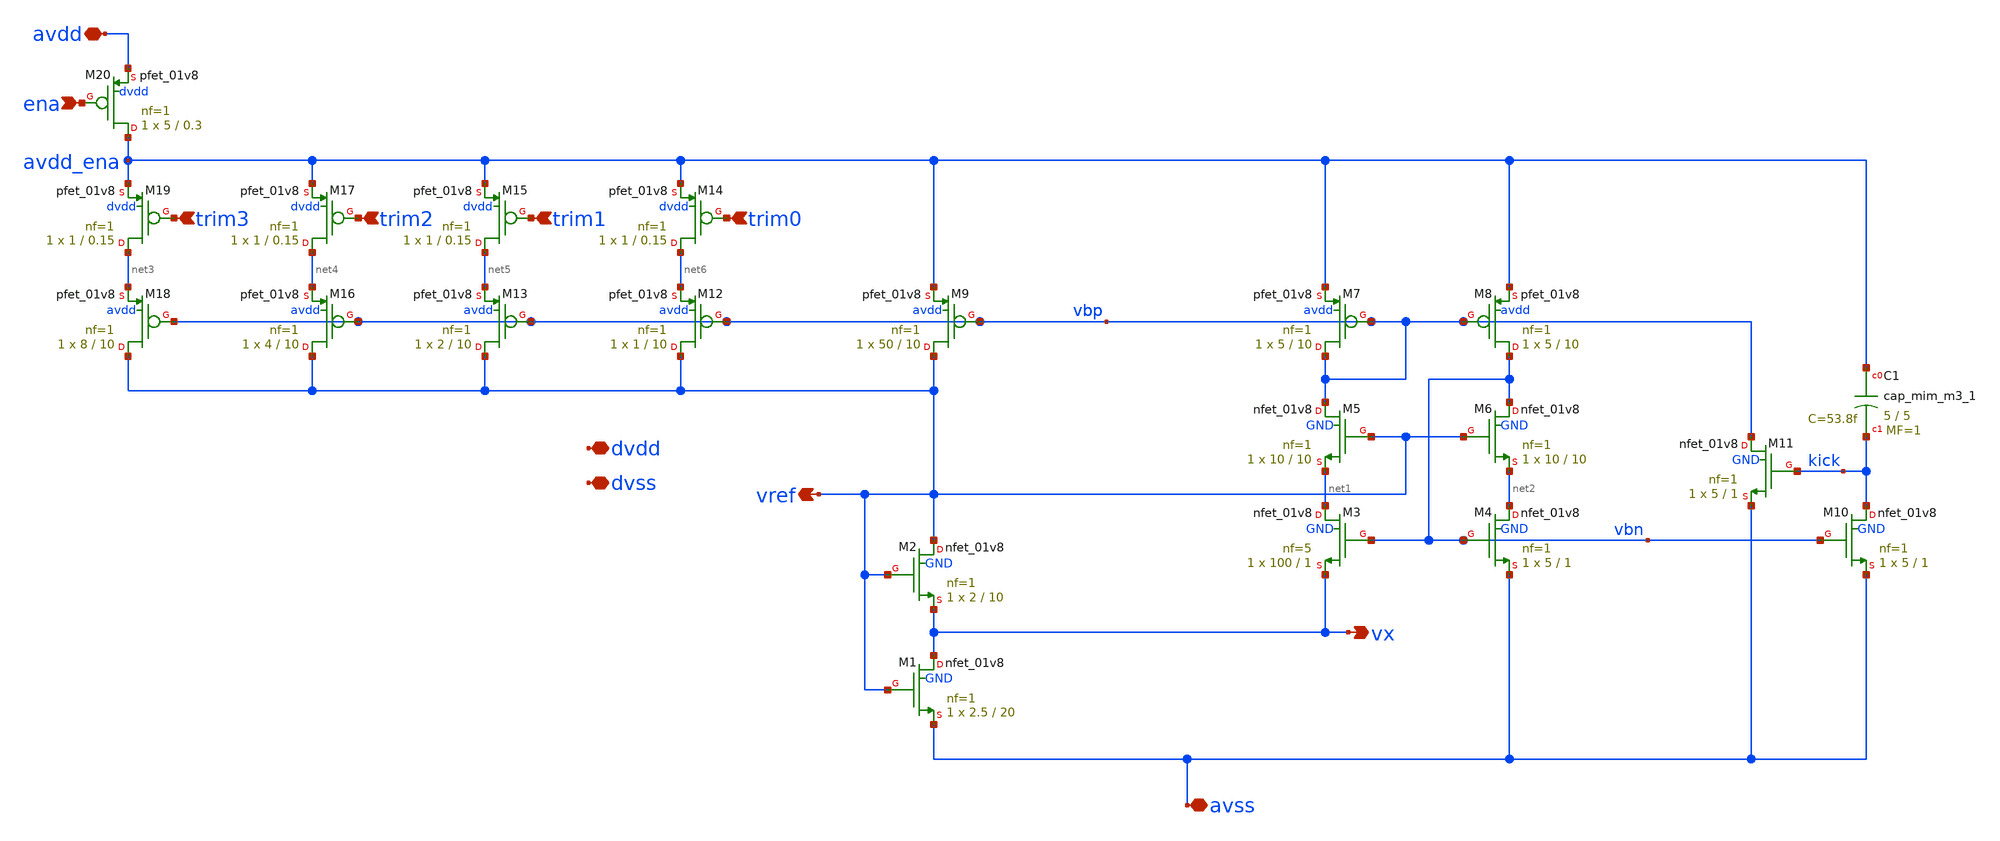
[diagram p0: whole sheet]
** sch_path: xschem/sky130_ak_ip__cmos_vref.sch
**.subckt sky130_ak_ip__cmos_vref vref avss avdd vx trim0 trim1 trim2 trim3 dvdd dvss ena
*.opin vref
*.iopin avss
*.iopin avdd
*.opin vx
*.ipin trim0
*.ipin trim1
*.ipin trim2
*.ipin trim3
*.iopin dvdd
*.iopin dvss
*.ipin ena
XM2 vref vref vx GND sky130_fd_pr__nfet_01v8 L=10 W=2 nf=1 ad='int((nf+1)/2) * W/nf * 0.29' as='int((nf+2)/2) * W/nf * 0.29'
+ pd='2*int((nf+1)/2) * (W/nf + 0.29)' ps='2*int((nf+2)/2) * (W/nf + 0.29)' nrd='0.29 / W' nrs='0.29 / W'
+ sa=0 sb=0 sd=0 mult=1 m=1
XM1 vx vref avss GND sky130_fd_pr__nfet_01v8 L=20 W=2.5 nf=1 ad='int((nf+1)/2) * W/nf * 0.29' as='int((nf+2)/2) * W/nf * 0.29'
+ pd='2*int((nf+1)/2) * (W/nf + 0.29)' ps='2*int((nf+2)/2) * (W/nf + 0.29)' nrd='0.29 / W' nrs='0.29 / W'
+ sa=0 sb=0 sd=0 mult=1 m=1
XM3 net1 vbn vx GND sky130_fd_pr__nfet_01v8 L=1 W=100 nf=5 ad='int((nf+1)/2) * W/nf * 0.29' as='int((nf+2)/2) * W/nf * 0.29'
+ pd='2*int((nf+1)/2) * (W/nf + 0.29)' ps='2*int((nf+2)/2) * (W/nf + 0.29)' nrd='0.29 / W' nrs='0.29 / W'
+ sa=0 sb=0 sd=0 mult=1 m=1
XM4 net2 vbn avss GND sky130_fd_pr__nfet_01v8 L=1 W=5 nf=1 ad='int((nf+1)/2) * W/nf * 0.29' as='int((nf+2)/2) * W/nf * 0.29'
+ pd='2*int((nf+1)/2) * (W/nf + 0.29)' ps='2*int((nf+2)/2) * (W/nf + 0.29)' nrd='0.29 / W' nrs='0.29 / W'
+ sa=0 sb=0 sd=0 mult=1 m=1
XM5 vbp vref net1 GND sky130_fd_pr__nfet_01v8 L=10 W=10 nf=1 ad='int((nf+1)/2) * W/nf * 0.29' as='int((nf+2)/2) * W/nf * 0.29'
+ pd='2*int((nf+1)/2) * (W/nf + 0.29)' ps='2*int((nf+2)/2) * (W/nf + 0.29)' nrd='0.29 / W' nrs='0.29 / W'
+ sa=0 sb=0 sd=0 mult=1 m=1
XM6 vbn vref net2 GND sky130_fd_pr__nfet_01v8 L=10 W=10 nf=1 ad='int((nf+1)/2) * W/nf * 0.29' as='int((nf+2)/2) * W/nf * 0.29'
+ pd='2*int((nf+1)/2) * (W/nf + 0.29)' ps='2*int((nf+2)/2) * (W/nf + 0.29)' nrd='0.29 / W' nrs='0.29 / W'
+ sa=0 sb=0 sd=0 mult=1 m=1
XM7 vbp vbp avdd_ena avdd sky130_fd_pr__pfet_01v8 L=10 W=5 nf=1 ad='int((nf+1)/2) * W/nf * 0.29' as='int((nf+2)/2) * W/nf * 0.29'
+ pd='2*int((nf+1)/2) * (W/nf + 0.29)' ps='2*int((nf+2)/2) * (W/nf + 0.29)' nrd='0.29 / W' nrs='0.29 / W'
+ sa=0 sb=0 sd=0 mult=1 m=1
XM8 vbn vbp avdd_ena avdd sky130_fd_pr__pfet_01v8 L=10 W=5 nf=1 ad='int((nf+1)/2) * W/nf * 0.29' as='int((nf+2)/2) * W/nf * 0.29'
+ pd='2*int((nf+1)/2) * (W/nf + 0.29)' ps='2*int((nf+2)/2) * (W/nf + 0.29)' nrd='0.29 / W' nrs='0.29 / W'
+ sa=0 sb=0 sd=0 mult=1 m=1
XM9 vref vbp avdd_ena avdd sky130_fd_pr__pfet_01v8 L=10 W=50 nf=1 ad='int((nf+1)/2) * W/nf * 0.29' as='int((nf+2)/2) * W/nf * 0.29'
+ pd='2*int((nf+1)/2) * (W/nf + 0.29)' ps='2*int((nf+2)/2) * (W/nf + 0.29)' nrd='0.29 / W' nrs='0.29 / W'
+ sa=0 sb=0 sd=0 mult=1 m=1
XM10 kick vbn avss GND sky130_fd_pr__nfet_01v8 L=1 W=5 nf=1 ad='int((nf+1)/2) * W/nf * 0.29' as='int((nf+2)/2) * W/nf * 0.29'
+ pd='2*int((nf+1)/2) * (W/nf + 0.29)' ps='2*int((nf+2)/2) * (W/nf + 0.29)' nrd='0.29 / W' nrs='0.29 / W'
+ sa=0 sb=0 sd=0 mult=1 m=1
XM11 vbp kick avss GND sky130_fd_pr__nfet_01v8 L=1 W=5 nf=1 ad='int((nf+1)/2) * W/nf * 0.29' as='int((nf+2)/2) * W/nf * 0.29'
+ pd='2*int((nf+1)/2) * (W/nf + 0.29)' ps='2*int((nf+2)/2) * (W/nf + 0.29)' nrd='0.29 / W' nrs='0.29 / W'
+ sa=0 sb=0 sd=0 mult=1 m=1
XC1 avdd_ena kick sky130_fd_pr__cap_mim_m3_1 W=5 L=5 MF=1 m=1
XM12 vref vbp net6 avdd sky130_fd_pr__pfet_01v8 L=10 W=1 nf=1 ad='int((nf+1)/2) * W/nf * 0.29' as='int((nf+2)/2) * W/nf * 0.29'
+ pd='2*int((nf+1)/2) * (W/nf + 0.29)' ps='2*int((nf+2)/2) * (W/nf + 0.29)' nrd='0.29 / W' nrs='0.29 / W'
+ sa=0 sb=0 sd=0 mult=1 m=1
XM13 vref vbp net5 avdd sky130_fd_pr__pfet_01v8 L=10 W=2 nf=1 ad='int((nf+1)/2) * W/nf * 0.29' as='int((nf+2)/2) * W/nf * 0.29'
+ pd='2*int((nf+1)/2) * (W/nf + 0.29)' ps='2*int((nf+2)/2) * (W/nf + 0.29)' nrd='0.29 / W' nrs='0.29 / W'
+ sa=0 sb=0 sd=0 mult=1 m=1
XM14 net6 trim0 avdd_ena dvdd sky130_fd_pr__pfet_01v8 L=0.15 W=1 nf=1 ad='int((nf+1)/2) * W/nf * 0.29'
+ as='int((nf+2)/2) * W/nf * 0.29' pd='2*int((nf+1)/2) * (W/nf + 0.29)' ps='2*int((nf+2)/2) * (W/nf + 0.29)'
+ nrd='0.29 / W' nrs='0.29 / W' sa=0 sb=0 sd=0 mult=1 m=1
XM15 net5 trim1 avdd_ena dvdd sky130_fd_pr__pfet_01v8 L=0.15 W=1 nf=1 ad='int((nf+1)/2) * W/nf * 0.29'
+ as='int((nf+2)/2) * W/nf * 0.29' pd='2*int((nf+1)/2) * (W/nf + 0.29)' ps='2*int((nf+2)/2) * (W/nf + 0.29)'
+ nrd='0.29 / W' nrs='0.29 / W' sa=0 sb=0 sd=0 mult=1 m=1
XM16 vref vbp net4 avdd sky130_fd_pr__pfet_01v8 L=10 W=4 nf=1 ad='int((nf+1)/2) * W/nf * 0.29' as='int((nf+2)/2) * W/nf * 0.29'
+ pd='2*int((nf+1)/2) * (W/nf + 0.29)' ps='2*int((nf+2)/2) * (W/nf + 0.29)' nrd='0.29 / W' nrs='0.29 / W'
+ sa=0 sb=0 sd=0 mult=1 m=1
XM17 net4 trim2 avdd_ena dvdd sky130_fd_pr__pfet_01v8 L=0.15 W=1 nf=1 ad='int((nf+1)/2) * W/nf * 0.29'
+ as='int((nf+2)/2) * W/nf * 0.29' pd='2*int((nf+1)/2) * (W/nf + 0.29)' ps='2*int((nf+2)/2) * (W/nf + 0.29)'
+ nrd='0.29 / W' nrs='0.29 / W' sa=0 sb=0 sd=0 mult=1 m=1
XM18 vref vbp net3 avdd sky130_fd_pr__pfet_01v8 L=10 W=8 nf=1 ad='int((nf+1)/2) * W/nf * 0.29' as='int((nf+2)/2) * W/nf * 0.29'
+ pd='2*int((nf+1)/2) * (W/nf + 0.29)' ps='2*int((nf+2)/2) * (W/nf + 0.29)' nrd='0.29 / W' nrs='0.29 / W'
+ sa=0 sb=0 sd=0 mult=1 m=1
XM19 net3 trim3 avdd_ena dvdd sky130_fd_pr__pfet_01v8 L=0.15 W=1 nf=1 ad='int((nf+1)/2) * W/nf * 0.29'
+ as='int((nf+2)/2) * W/nf * 0.29' pd='2*int((nf+1)/2) * (W/nf + 0.29)' ps='2*int((nf+2)/2) * (W/nf + 0.29)'
+ nrd='0.29 / W' nrs='0.29 / W' sa=0 sb=0 sd=0 mult=1 m=1
XM20 avdd_ena ena avdd dvdd sky130_fd_pr__pfet_01v8 L=0.3 W=5 nf=1 ad='int((nf+1)/2) * W/nf * 0.29' as='int((nf+2)/2) * W/nf * 0.29'
+ pd='2*int((nf+1)/2) * (W/nf + 0.29)' ps='2*int((nf+2)/2) * (W/nf + 0.29)' nrd='0.29 / W' nrs='0.29 / W'
+ sa=0 sb=0 sd=0 mult=1 m=1
**.ends
.end
